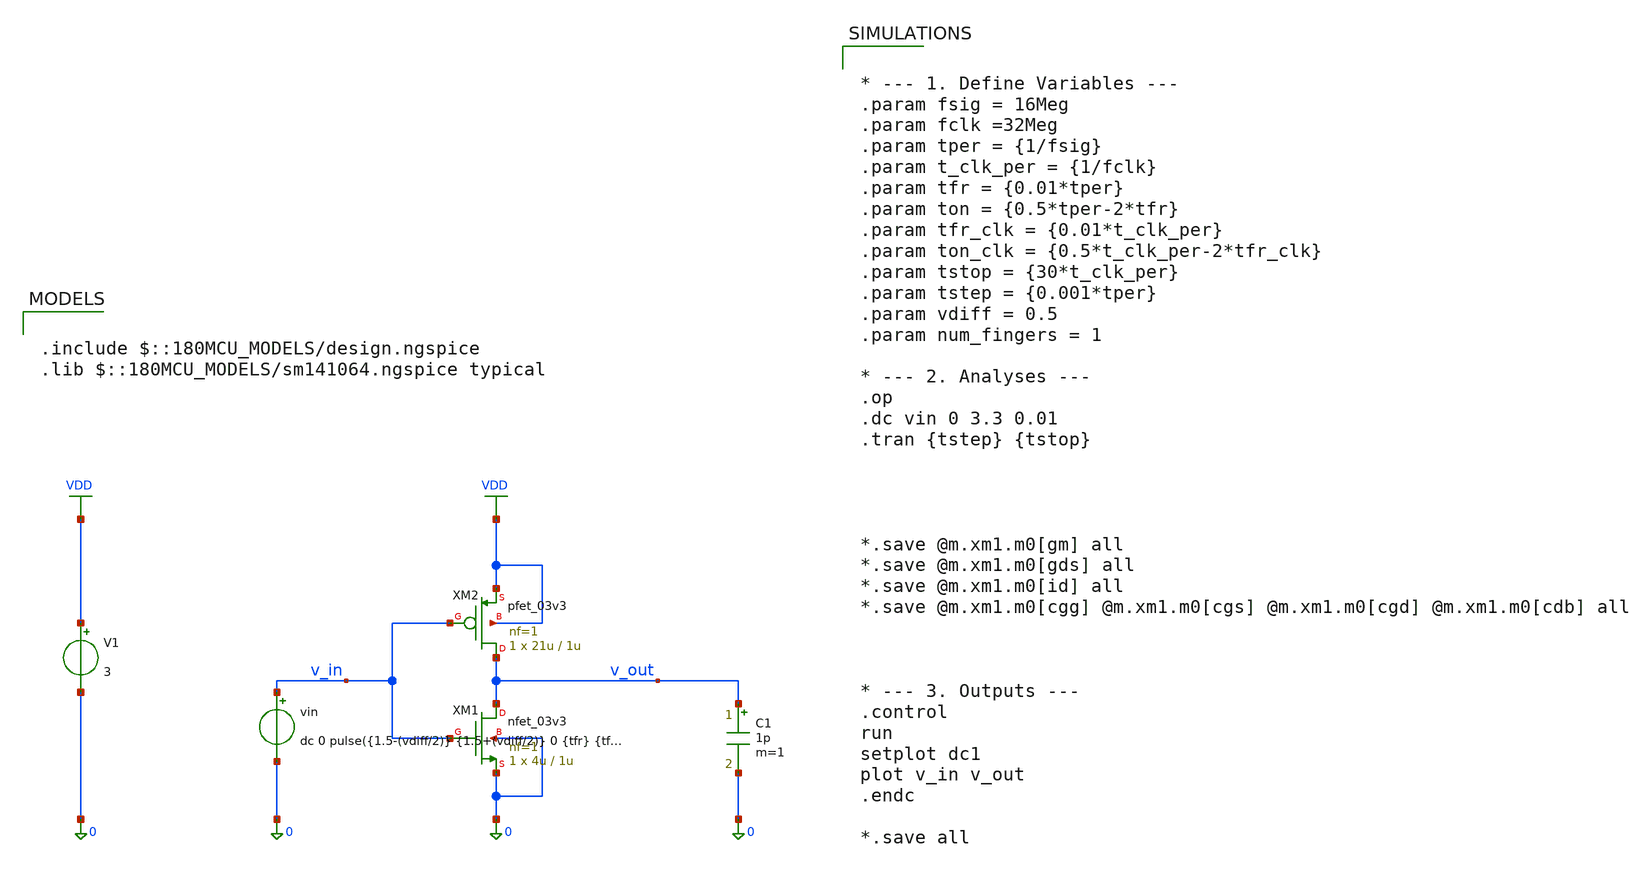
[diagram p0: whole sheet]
** sch_path: Felix/untitled-1.sch
**.subckt untitled-1
XM1 v_out v_in 0 0 nfet_03v3 L=1u W=4u nf=1 ad='int((nf+1)/2) * W/nf * 0.18u' as='int((nf+2)/2) * W/nf * 0.18u'
+ pd='2*int((nf+1)/2) * (W/nf + 0.18u)' ps='2*int((nf+2)/2) * (W/nf + 0.18u)' nrd='0.18u / W' nrs='0.18u / W'
+ sa=0 sb=0 sd=0 m=1
XM2 v_out v_in VDD VDD pfet_03v3 L=1u W=21u nf=1 ad='int((nf+1)/2) * W/nf * 0.18u' as='int((nf+2)/2) * W/nf * 0.18u'
+ pd='2*int((nf+1)/2) * (W/nf + 0.18u)' ps='2*int((nf+2)/2) * (W/nf + 0.18u)' nrd='0.18u / W' nrs='0.18u / W'
+ sa=0 sb=0 sd=0 m=1
V1 VDD 0 3
vin v_in 0 dc 0 pulse({1.5-(vdiff/2)} {1.5+(vdiff/2)} 0 {tfr} {tfr} {ton} {tper})
C1 v_out 0 1p m=1
**** begin user architecture code


* --- 1. Define Variables ---
.param fsig = 16Meg
.param fclk =32Meg
.param tper = {1/fsig}
.param t_clk_per = {1/fclk}
.param tfr = {0.01*tper}
.param ton = {0.5*tper-2*tfr}
.param tfr_clk = {0.01*t_clk_per}
.param ton_clk = {0.5*t_clk_per-2*tfr_clk}
.param tstop = {30*t_clk_per}
.param tstep = {0.001*tper}
.param vdiff = 0.5
.param num_fingers = 1

* --- 2. Analyses ---
.op
.dc vin 0 3.3 0.01
.tran {tstep} {tstop}




*.save @m.xm1.m0[gm] all
*.save @m.xm1.m0[gds] all
*.save @m.xm1.m0[id] all
*.save @m.xm1.m0[cgg] @m.xm1.m0[cgs] @m.xm1.m0[cgd] @m.xm1.m0[cdb] all



* --- 3. Outputs ---
.control
run
setplot dc1
plot v_in v_out
.endc

*.save all



.include $::180MCU_MODELS/design.ngspice
.lib $::180MCU_MODELS/sm141064.ngspice typical

**** end user architecture code
**.ends
.GLOBAL VDD
.end
